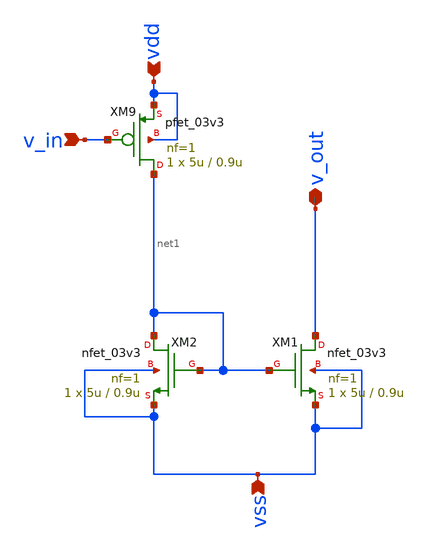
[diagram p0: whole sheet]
** sch_path: blocks/composite/regulated_cascoded_cmirror/xschem/vanilla_cm.sch
**.subckt vanilla_cm v_in vdd vss v_out
*.ipin v_in
*.ipin vdd
*.ipin vss
*.iopin v_out
XM1 v_out net1 vss vss nfet_03v3 L=0.9u W=5u nf=1 ad='int((nf+1)/2) * W/nf * 0.18u' as='int((nf+2)/2) * W/nf * 0.18u'
+ pd='2*int((nf+1)/2) * (W/nf + 0.18u)' ps='2*int((nf+2)/2) * (W/nf + 0.18u)' nrd='0.18u / W' nrs='0.18u / W'
+ sa=0 sb=0 sd=0 m=1
XM2 net1 net1 vss vss nfet_03v3 L=0.9u W=5u nf=1 ad='int((nf+1)/2) * W/nf * 0.18u' as='int((nf+2)/2) * W/nf * 0.18u'
+ pd='2*int((nf+1)/2) * (W/nf + 0.18u)' ps='2*int((nf+2)/2) * (W/nf + 0.18u)' nrd='0.18u / W' nrs='0.18u / W'
+ sa=0 sb=0 sd=0 m=1
XM9 net1 v_in vdd vdd pfet_03v3 L=0.9u W=5u nf=1 ad='int((nf+1)/2) * W/nf * 0.18u' as='int((nf+2)/2) * W/nf * 0.18u'
+ pd='2*int((nf+1)/2) * (W/nf + 0.18u)' ps='2*int((nf+2)/2) * (W/nf + 0.18u)' nrd='0.18u / W' nrs='0.18u / W'
+ sa=0 sb=0 sd=0 m=1
**.ends
.end
